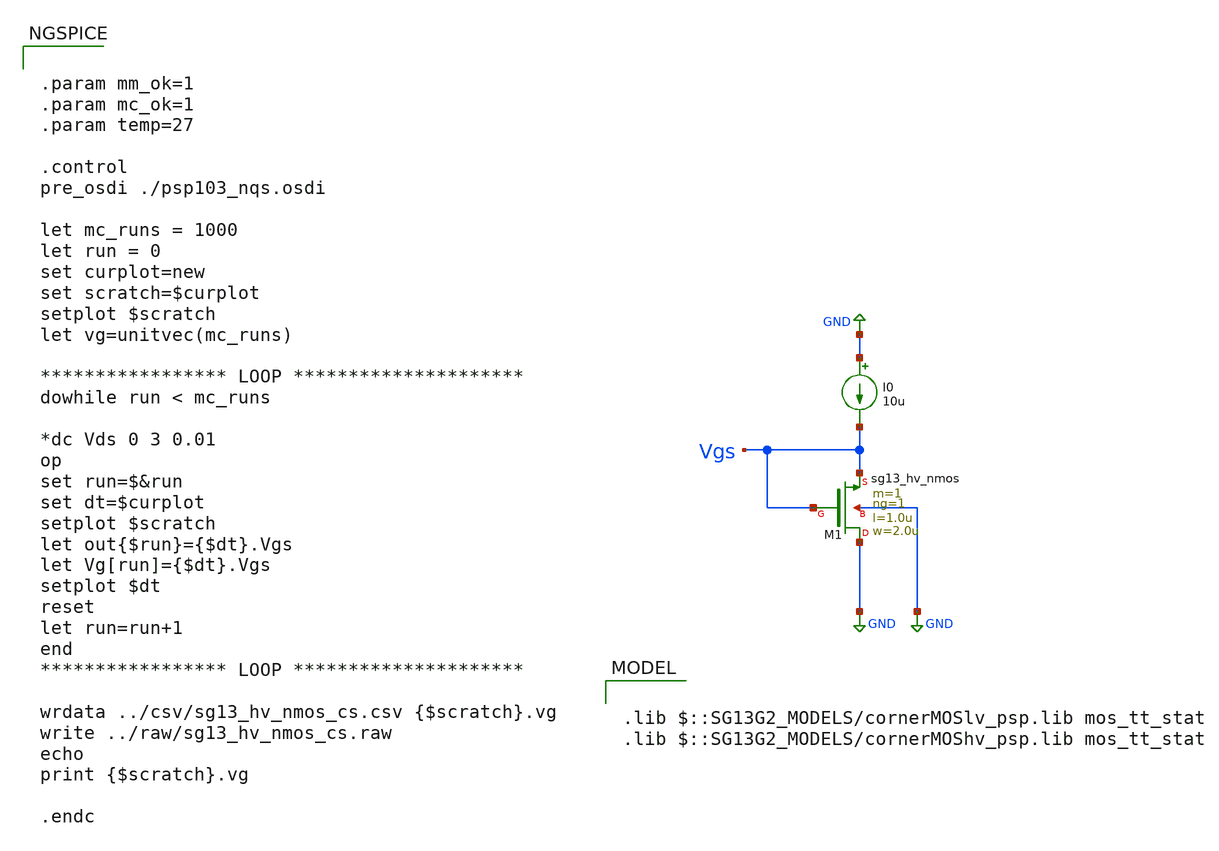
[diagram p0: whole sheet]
** sch_path: ihp-sg13g2/libs.tech/xschem/sg13g2_tests/mc_hv_nmos_cs_loop.sch
* Copyright 2023 IHP PDK Authors
**.subckt mc_hv_nmos_cs_loop
I0 GND Vgs 10u
XM1 GND Vgs Vgs GND sg13_hv_nmos w=2.0u l=1.0u ng=1 m=1 mm_ok=1
**** begin user architecture code

.lib $::SG13G2_MODELS/cornerMOSlv_psp.lib mos_tt_stat
.lib $::SG13G2_MODELS/cornerMOShv_psp.lib mos_tt_stat




.param mm_ok=1
.param mc_ok=1
.param temp=27

.control
pre_osdi ./psp103_nqs.osdi

let mc_runs = 1000
let run = 0
set curplot=new
set scratch=$curplot
setplot $scratch
let vg=unitvec(mc_runs)

***************** LOOP *********************
dowhile run < mc_runs

*dc Vds 0 3 0.01
op
set run=$&run
set dt=$curplot
setplot $scratch
let out{$run}={$dt}.Vgs
let Vg[run]={$dt}.Vgs
setplot $dt
reset
let run=run+1
end
***************** LOOP *********************

wrdata ../csv/sg13_hv_nmos_cs.csv {$scratch}.vg
write ../raw/sg13_hv_nmos_cs.raw
echo
print {$scratch}.vg

.endc


**** end user architecture code
**.ends
.GLOBAL GND
.end
